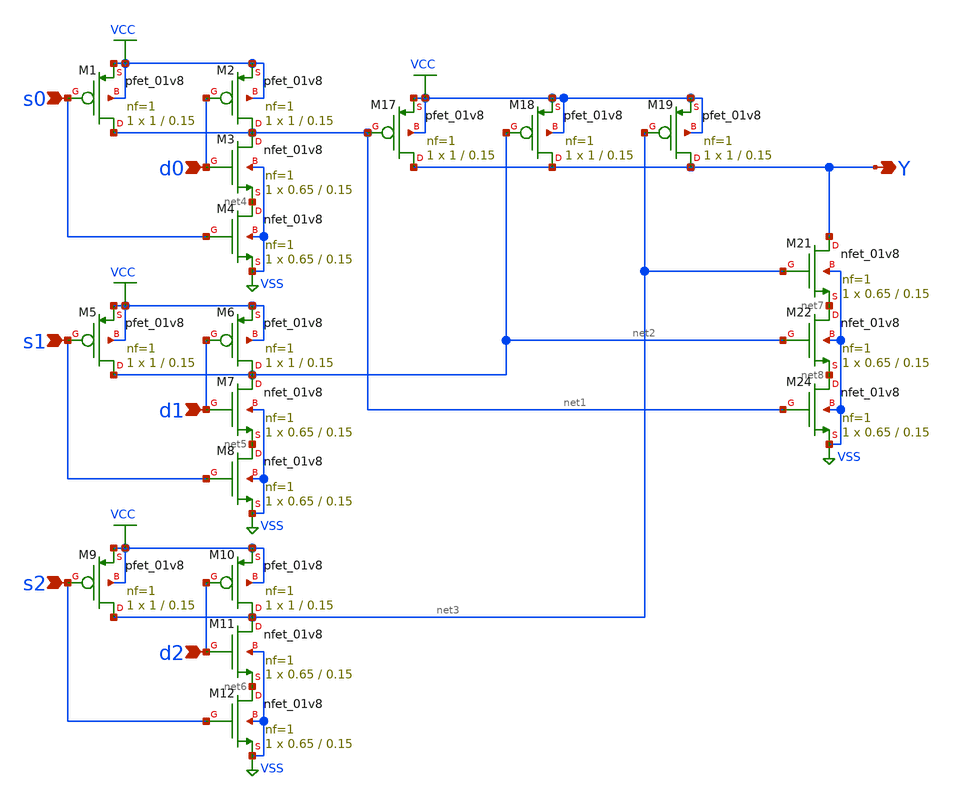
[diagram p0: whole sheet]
** sch_path: elements/logic/mux3.sch
**.subckt mux3 s0 d0 s1 d1 s2 d2 Y
*.ipin s0
*.ipin d0
*.ipin s1
*.ipin d1
*.ipin s2
*.ipin d2
*.opin Y
XM1 net1 s0 VCC VCC sky130_fd_pr__pfet_01v8 L=0.15 W=1 nf=1 ad='int((nf+1)/2) * W/nf * 0.29' as='int((nf+2)/2) * W/nf * 0.29'
+ pd='2*int((nf+1)/2) * (W/nf + 0.29)' ps='2*int((nf+2)/2) * (W/nf + 0.29)' nrd='0.29 / W' nrs='0.29 / W'
+ sa=0 sb=0 sd=0 mult=1 m=1
XM2 net1 d0 VCC VCC sky130_fd_pr__pfet_01v8 L=0.15 W=1 nf=1 ad='int((nf+1)/2) * W/nf * 0.29' as='int((nf+2)/2) * W/nf * 0.29'
+ pd='2*int((nf+1)/2) * (W/nf + 0.29)' ps='2*int((nf+2)/2) * (W/nf + 0.29)' nrd='0.29 / W' nrs='0.29 / W'
+ sa=0 sb=0 sd=0 mult=1 m=1
XM3 net1 d0 net4 VSS sky130_fd_pr__nfet_01v8 L=0.15 W=0.65 nf=1 ad='int((1 + 1)/2) * 0.65 / 1 * 0.29'
+ as='int((1 + 2)/2) * 0.65 / 1 * 0.29' pd='2*int((1 + 1)/2) * (0.65 / 1 + 0.29)' ps='2*int((1 + 2)/2) * (0.65 / 1 + 0.29)'
+ nrd='0.29 / 0.65 ' nrs='0.29 / 0.65 ' sa=0 sb=0 sd=0 mult=1 m=1
XM4 net4 s0 VSS VSS sky130_fd_pr__nfet_01v8 L=0.15 W=0.65 nf=1 ad='int((1 + 1)/2) * 0.65 / 1 * 0.29'
+ as='int((1 + 2)/2) * 0.65 / 1 * 0.29' pd='2*int((1 + 1)/2) * (0.65 / 1 + 0.29)' ps='2*int((1 + 2)/2) * (0.65 / 1 + 0.29)'
+ nrd='0.29 / 0.65 ' nrs='0.29 / 0.65 ' sa=0 sb=0 sd=0 mult=1 m=1
XM5 net2 s1 VCC VCC sky130_fd_pr__pfet_01v8 L=0.15 W=1 nf=1 ad='int((nf+1)/2) * W/nf * 0.29' as='int((nf+2)/2) * W/nf * 0.29'
+ pd='2*int((nf+1)/2) * (W/nf + 0.29)' ps='2*int((nf+2)/2) * (W/nf + 0.29)' nrd='0.29 / W' nrs='0.29 / W'
+ sa=0 sb=0 sd=0 mult=1 m=1
XM6 net2 d1 VCC VCC sky130_fd_pr__pfet_01v8 L=0.15 W=1 nf=1 ad='int((nf+1)/2) * W/nf * 0.29' as='int((nf+2)/2) * W/nf * 0.29'
+ pd='2*int((nf+1)/2) * (W/nf + 0.29)' ps='2*int((nf+2)/2) * (W/nf + 0.29)' nrd='0.29 / W' nrs='0.29 / W'
+ sa=0 sb=0 sd=0 mult=1 m=1
XM7 net2 d1 net5 VSS sky130_fd_pr__nfet_01v8 L=0.15 W=0.65 nf=1 ad='int((1 + 1)/2) * 0.65 / 1 * 0.29'
+ as='int((1 + 2)/2) * 0.65 / 1 * 0.29' pd='2*int((1 + 1)/2) * (0.65 / 1 + 0.29)' ps='2*int((1 + 2)/2) * (0.65 / 1 + 0.29)'
+ nrd='0.29 / 0.65 ' nrs='0.29 / 0.65 ' sa=0 sb=0 sd=0 mult=1 m=1
XM8 net5 s1 VSS VSS sky130_fd_pr__nfet_01v8 L=0.15 W=0.65 nf=1 ad='int((1 + 1)/2) * 0.65 / 1 * 0.29'
+ as='int((1 + 2)/2) * 0.65 / 1 * 0.29' pd='2*int((1 + 1)/2) * (0.65 / 1 + 0.29)' ps='2*int((1 + 2)/2) * (0.65 / 1 + 0.29)'
+ nrd='0.29 / 0.65 ' nrs='0.29 / 0.65 ' sa=0 sb=0 sd=0 mult=1 m=1
XM9 net3 s2 VCC VCC sky130_fd_pr__pfet_01v8 L=0.15 W=1 nf=1 ad='int((nf+1)/2) * W/nf * 0.29' as='int((nf+2)/2) * W/nf * 0.29'
+ pd='2*int((nf+1)/2) * (W/nf + 0.29)' ps='2*int((nf+2)/2) * (W/nf + 0.29)' nrd='0.29 / W' nrs='0.29 / W'
+ sa=0 sb=0 sd=0 mult=1 m=1
XM10 net3 d2 VCC VCC sky130_fd_pr__pfet_01v8 L=0.15 W=1 nf=1 ad='int((nf+1)/2) * W/nf * 0.29' as='int((nf+2)/2) * W/nf * 0.29'
+ pd='2*int((nf+1)/2) * (W/nf + 0.29)' ps='2*int((nf+2)/2) * (W/nf + 0.29)' nrd='0.29 / W' nrs='0.29 / W'
+ sa=0 sb=0 sd=0 mult=1 m=1
XM11 net3 d2 net6 VSS sky130_fd_pr__nfet_01v8 L=0.15 W=0.65 nf=1 ad='int((1 + 1)/2) * 0.65 / 1 * 0.29'
+ as='int((1 + 2)/2) * 0.65 / 1 * 0.29' pd='2*int((1 + 1)/2) * (0.65 / 1 + 0.29)' ps='2*int((1 + 2)/2) * (0.65 / 1 + 0.29)'
+ nrd='0.29 / 0.65 ' nrs='0.29 / 0.65 ' sa=0 sb=0 sd=0 mult=1 m=1
XM12 net6 s2 VSS VSS sky130_fd_pr__nfet_01v8 L=0.15 W=0.65 nf=1 ad='int((1 + 1)/2) * 0.65 / 1 * 0.29'
+ as='int((1 + 2)/2) * 0.65 / 1 * 0.29' pd='2*int((1 + 1)/2) * (0.65 / 1 + 0.29)' ps='2*int((1 + 2)/2) * (0.65 / 1 + 0.29)'
+ nrd='0.29 / 0.65 ' nrs='0.29 / 0.65 ' sa=0 sb=0 sd=0 mult=1 m=1
XM17 Y net1 VCC VCC sky130_fd_pr__pfet_01v8 L=0.15 W=1 nf=1 ad='int((nf+1)/2) * W/nf * 0.29' as='int((nf+2)/2) * W/nf * 0.29'
+ pd='2*int((nf+1)/2) * (W/nf + 0.29)' ps='2*int((nf+2)/2) * (W/nf + 0.29)' nrd='0.29 / W' nrs='0.29 / W'
+ sa=0 sb=0 sd=0 mult=1 m=1
XM18 Y net2 VCC VCC sky130_fd_pr__pfet_01v8 L=0.15 W=1 nf=1 ad='int((nf+1)/2) * W/nf * 0.29' as='int((nf+2)/2) * W/nf * 0.29'
+ pd='2*int((nf+1)/2) * (W/nf + 0.29)' ps='2*int((nf+2)/2) * (W/nf + 0.29)' nrd='0.29 / W' nrs='0.29 / W'
+ sa=0 sb=0 sd=0 mult=1 m=1
XM19 Y net3 VCC VCC sky130_fd_pr__pfet_01v8 L=0.15 W=1 nf=1 ad='int((nf+1)/2) * W/nf * 0.29' as='int((nf+2)/2) * W/nf * 0.29'
+ pd='2*int((nf+1)/2) * (W/nf + 0.29)' ps='2*int((nf+2)/2) * (W/nf + 0.29)' nrd='0.29 / W' nrs='0.29 / W'
+ sa=0 sb=0 sd=0 mult=1 m=1
XM21 Y net3 net7 VSS sky130_fd_pr__nfet_01v8 L=0.15 W=0.65 nf=1 ad='int((1 + 1)/2) * 0.65 / 1 * 0.29'
+ as='int((1 + 2)/2) * 0.65 / 1 * 0.29' pd='2*int((1 + 1)/2) * (0.65 / 1 + 0.29)' ps='2*int((1 + 2)/2) * (0.65 / 1 + 0.29)'
+ nrd='0.29 / 0.65 ' nrs='0.29 / 0.65 ' sa=0 sb=0 sd=0 mult=1 m=1
XM22 net7 net2 net8 VSS sky130_fd_pr__nfet_01v8 L=0.15 W=0.65 nf=1 ad='int((1 + 1)/2) * 0.65 / 1 * 0.29'
+ as='int((1 + 2)/2) * 0.65 / 1 * 0.29' pd='2*int((1 + 1)/2) * (0.65 / 1 + 0.29)' ps='2*int((1 + 2)/2) * (0.65 / 1 + 0.29)'
+ nrd='0.29 / 0.65 ' nrs='0.29 / 0.65 ' sa=0 sb=0 sd=0 mult=1 m=1
XM24 net8 net1 VSS VSS sky130_fd_pr__nfet_01v8 L=0.15 W=0.65 nf=1 ad='int((1 + 1)/2) * 0.65 / 1 * 0.29'
+ as='int((1 + 2)/2) * 0.65 / 1 * 0.29' pd='2*int((1 + 1)/2) * (0.65 / 1 + 0.29)' ps='2*int((1 + 2)/2) * (0.65 / 1 + 0.29)'
+ nrd='0.29 / 0.65 ' nrs='0.29 / 0.65 ' sa=0 sb=0 sd=0 mult=1 m=1
**.ends
.GLOBAL VCC
.GLOBAL VSS
.end
